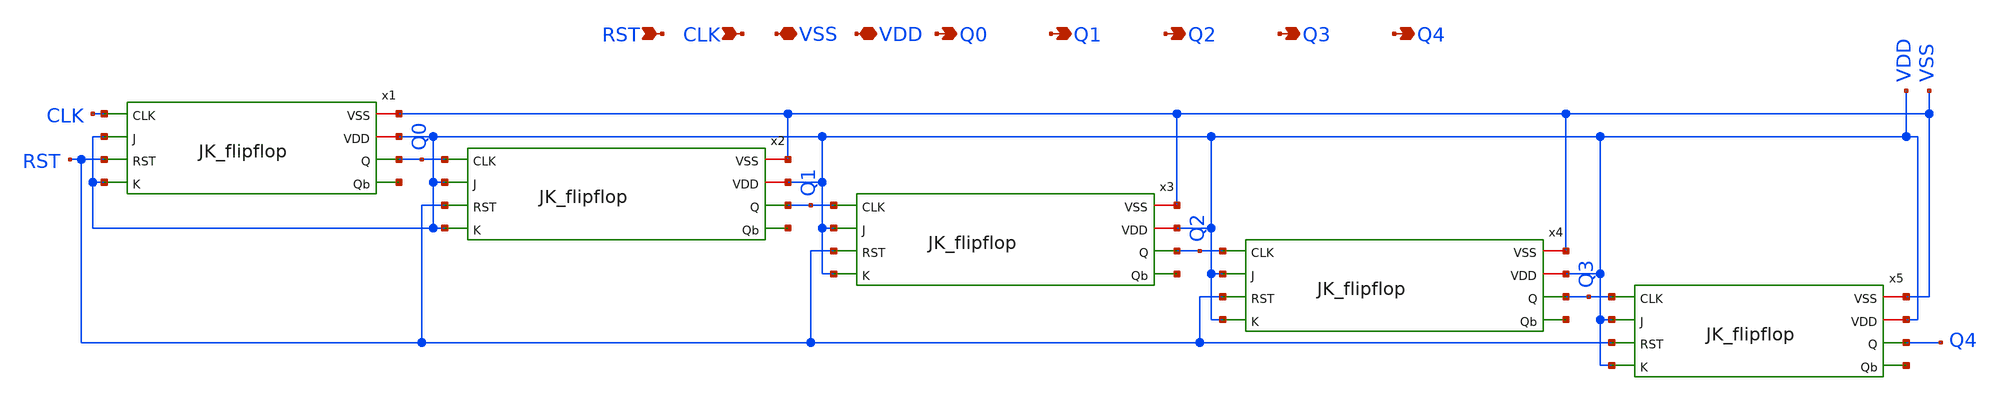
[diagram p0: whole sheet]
** sch_path: Clock_Generator_PAKISTAN_02/Schematics/CLK_div_32.sch
**.subckt CLK_div_32 CLK VSS VDD Q0 Q1 Q2 Q3 Q4 RST
*.ipin CLK
*.iopin VSS
*.iopin VDD
*.opin Q0
*.opin Q1
*.opin Q2
*.opin Q3
*.opin Q4
*.ipin RST
x1 CLK VSS VDD Q0 VDD net1 RST VDD JK_flipflop
x2 Q0 VSS VDD Q1 VDD net2 RST VDD JK_flipflop
x3 Q1 VSS VDD Q2 VDD net3 RST VDD JK_flipflop
x4 Q2 VSS VDD Q3 VDD net4 RST VDD JK_flipflop
x5 Q3 VSS VDD Q4 VDD net5 RST VDD JK_flipflop
**.ends
.end
